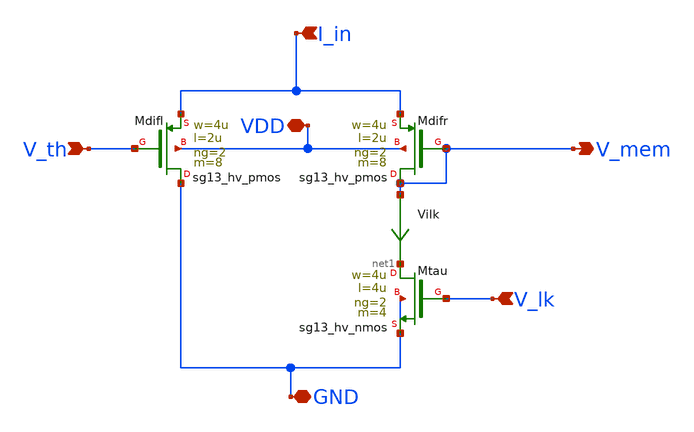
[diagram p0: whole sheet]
** sch_path: xschem/DPI.sch
**.subckt DPI V_mem V_lk V_th I_in VDD GND
*.opin V_mem
*.ipin V_lk
*.ipin V_th
*.ipin I_in
*.iopin VDD
*.iopin GND
XMdifl GND V_th I_in VDD sg13_hv_pmos w=4u l=2u ng=2 m=8 mm_ok=1
XMdifr V_mem V_mem I_in VDD sg13_hv_pmos w=4u l=2u ng=2 m=8 mm_ok=1
XMtau net1 V_lk GND GND sg13_hv_nmos w=4u l=4u ng=2 m=4 mm_ok=1
Vilk V_mem net1 0
.save i(vilk)
**.ends
.end
